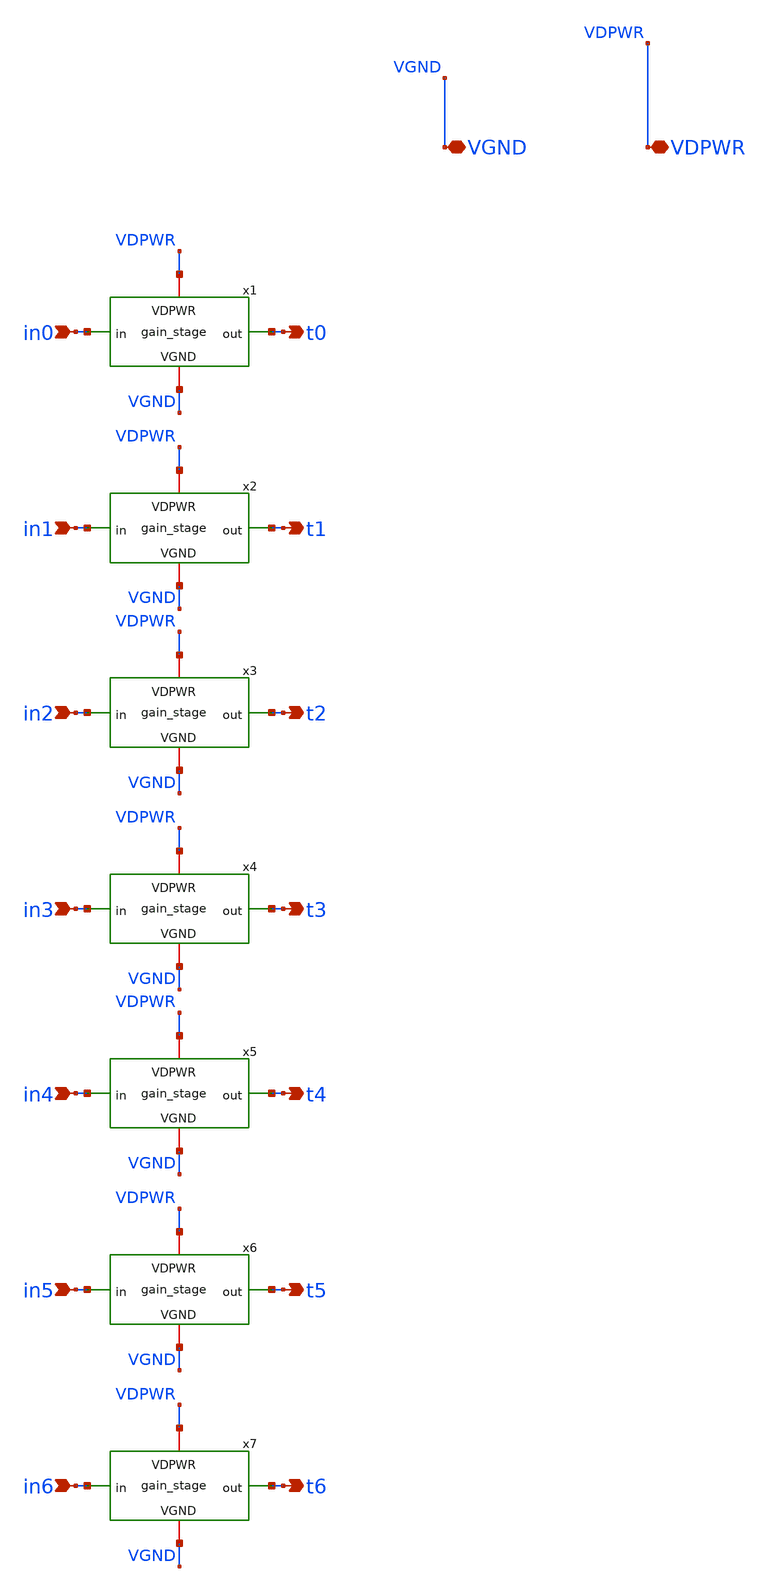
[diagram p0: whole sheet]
** sch_path: tt_um_emmersonv_tiq_adc/xschem/gain_stage_7.sch
**.subckt gain_stage_7 VGND VDPWR in0 in1 in2 in3 in4 in5 in6 t0 t1 t2 t3 t4 t5 t6
*.iopin VGND
*.iopin VDPWR
*.ipin in0
*.ipin in1
*.ipin in2
*.ipin in3
*.ipin in4
*.ipin in5
*.ipin in6
*.opin t0
*.opin t1
*.opin t2
*.opin t3
*.opin t4
*.opin t5
*.opin t6
x1 VDPWR VGND t0 in0 gain_stage
x2 VDPWR VGND t1 in1 gain_stage
x3 VDPWR VGND t2 in2 gain_stage
x4 VDPWR VGND t3 in3 gain_stage
x5 VDPWR VGND t4 in4 gain_stage
x6 VDPWR VGND t5 in5 gain_stage
x7 VDPWR VGND t6 in6 gain_stage
**.ends

* expanding   symbol:  gain_stage.sym # of pins=4
** sym_path: tt_um_emmersonv_tiq_adc/xschem/gain_stage.sym
** sch_path: tt_um_emmersonv_tiq_adc/xschem/gain_stage.sch
.subckt gain_stage VDPWR VGND out in
*.ipin in
*.opin out
*.iopin VGND
*.iopin VDPWR
x8 VDPWR net1 in VGND inverter_p1_n0o42
x9 VDPWR net2 net1 VGND inverter_p1_n0o42
x10 VDPWR out net2 VGND inverter_p1_n0o42
.ends


* expanding   symbol:
*+  /foss/designs/analog-circuit-design/sky25a-TIQ_ADC/xschem/INVERTER_SIZES/inverter_p1_n0o42.sym # of pins=4
** sym_path: tt_um_emmersonv_tiq_adc/xschem/INVERTER_SIZES/inverter_p1_n0o42.sym
** sch_path: tt_um_emmersonv_tiq_adc/xschem/INVERTER_SIZES/inverter_p1_n0o42.sch
.subckt inverter_p1_n0o42 VDPWR Vout Vin VGND
*.opin Vout
*.ipin Vin
*.iopin VDPWR
*.iopin VGND
XM1 Vout Vin VGND VGND sky130_fd_pr__nfet_01v8 L=0.15 W=0.42 nf=1 ad='int((nf+1)/2) * W/nf * 0.29' as='int((nf+2)/2) * W/nf * 0.29'
+ pd='2*int((nf+1)/2) * (W/nf + 0.29)' ps='2*int((nf+2)/2) * (W/nf + 0.29)' nrd='0.29 / W' nrs='0.29 / W'
+ sa=0 sb=0 sd=0 mult=1 m=1
XM2 Vout Vin VDPWR VDPWR sky130_fd_pr__pfet_01v8 L=0.15 W=1 nf=1 ad='int((nf+1)/2) * W/nf * 0.29' as='int((nf+2)/2) * W/nf * 0.29'
+ pd='2*int((nf+1)/2) * (W/nf + 0.29)' ps='2*int((nf+2)/2) * (W/nf + 0.29)' nrd='0.29 / W' nrs='0.29 / W'
+ sa=0 sb=0 sd=0 mult=1 m=1
.ends

.end
